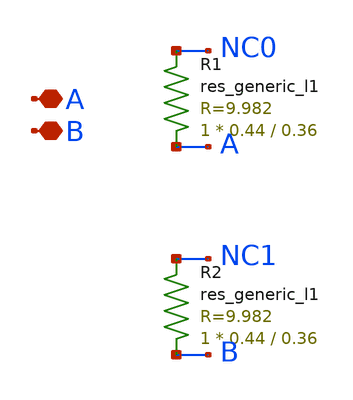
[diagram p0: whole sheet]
** sch_path: design/SUN_TR_SKY130NM/SUNTR_DCAPX1_CV.sch
**.subckt SUNTR_DCAPX1_CV A B
*.iopin A
*.iopin B
R1 A NC0 sky130_fd_pr__res_generic_l1 W=0.44 L=0.36 m=1
R2 B NC1 sky130_fd_pr__res_generic_l1 W=0.44 L=0.36 m=1
**.ends
.end
